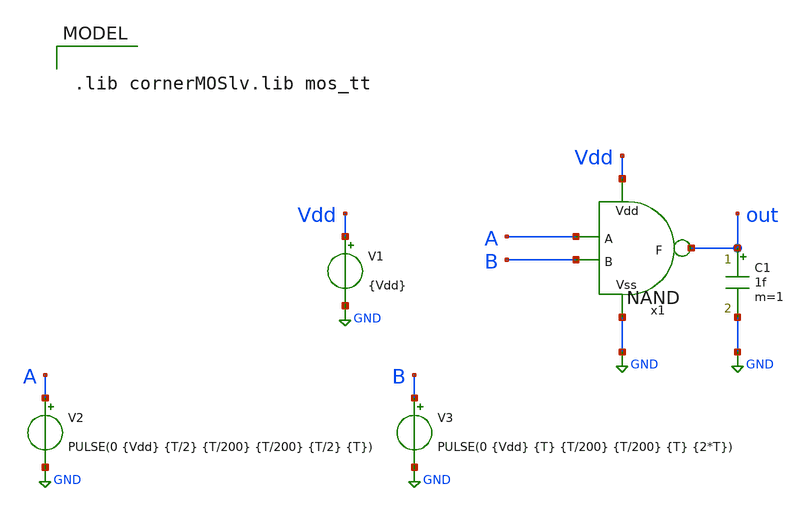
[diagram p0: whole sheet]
** sch_path: xschem/LogicGates/TB_NAND.sch
**.subckt TB_NAND
V1 Vdd GND {Vdd}
C1 out GND 1f m=1
x1 Vdd A B out GND NAND
V2 A GND PULSE(0 {Vdd} {T/2} {T/200} {T/200} {T/2} {T})
V3 B GND PULSE(0 {Vdd} {T} {T/200} {T/200} {T} {2*T})
**** begin user architecture code



.control
save all

tran 10p 10n

meas tran Propagacion_High_LOW TRIG v(a) VAL=0.6 RISE=2 TARG v(out) VAL=0.6 FALL=1
plot v(A) v(B) (v(out) + 1.2)
.endc





.lib cornerMOSlv.lib mos_tt



.param T = 2n
.param Vdd = 1.2
.param W_n = 1u
.param W_p = 1u


**** end user architecture code
**.ends

* expanding   symbol:  /foss/designs/Campamento-ChipUSM-2025/xschem/LogicGates/NAND.sym # of pins=5
** sym_path: xschem/LogicGates/NAND.sym
** sch_path: xschem/LogicGates/NAND.sch
.subckt NAND Vdd A B F Vss
*.ipin Vss
*.ipin A
*.ipin B
*.ipin Vdd
*.opin F
XM1 F B net1 Vss sg13_lv_nmos w={W_n} l=0.13u ng=1 m=1 mm_ok=1
XM2 net1 A Vss Vss sg13_lv_nmos w={W_n} l=0.13u ng=1 m=1 mm_ok=1
XM3 F B Vdd Vdd sg13_lv_pmos w={W_p} l=0.13u ng=1 m=1 mm_ok=1
XM4 F A Vdd Vdd sg13_lv_pmos w={W_n} l=0.13u ng=1 m=1 mm_ok=1
.ends

.GLOBAL GND
.end
